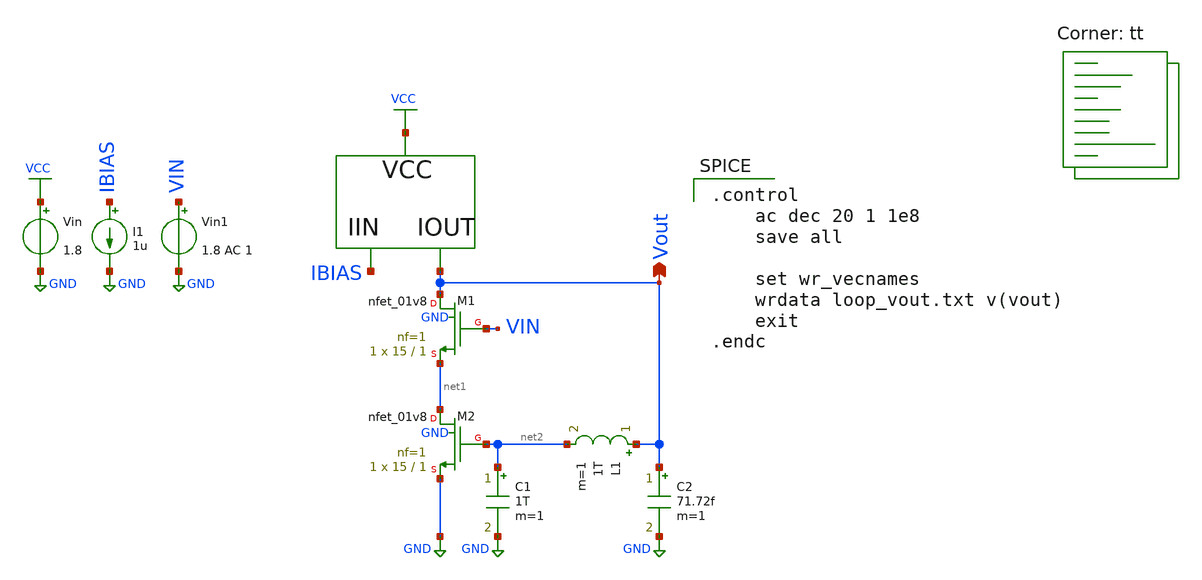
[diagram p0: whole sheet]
** sch_path: xschem/fvf_tb_loop.sch
**.subckt fvf_tb_loop Vout
*.opin Vout
Vin VCC GND 1.8
Vin1 VIN GND 1.8 AC 1
I1 IBIAS GND 1u
XM1 Vout VIN net1 GND sky130_fd_pr__nfet_01v8 L=1 W=15 nf=1 ad='int((nf+1)/2) * W/nf * 0.29' as='int((nf+2)/2) * W/nf * 0.29'
+ pd='2*int((nf+1)/2) * (W/nf + 0.29)' ps='2*int((nf+2)/2) * (W/nf + 0.29)' nrd='0.29 / W' nrs='0.29 / W'
+ sa=0 sb=0 sd=0 mult=1 m=1
XM2 net1 net2 GND GND sky130_fd_pr__nfet_01v8 L=1 W=15 nf=1 ad='int((nf+1)/2) * W/nf * 0.29' as='int((nf+2)/2) * W/nf * 0.29'
+ pd='2*int((nf+1)/2) * (W/nf + 0.29)' ps='2*int((nf+2)/2) * (W/nf + 0.29)' nrd='0.29 / W' nrs='0.29 / W'
+ sa=0 sb=0 sd=0 mult=1 m=1
L1 Vout net2 1T m=1
C1 net2 GND 1T m=1
C2 Vout GND 71.72f m=1
**** begin user architecture code
.lib $::SKYWATER_MODELS/sky130.lib.spice tt

.control
    ac dec 20 1 1e8
    save all

    set wr_vecnames
    wrdata loop_vout.txt v(vout)
    exit
.endc

**** end user architecture code
**.ends
.GLOBAL VCC
.GLOBAL GND
.end
